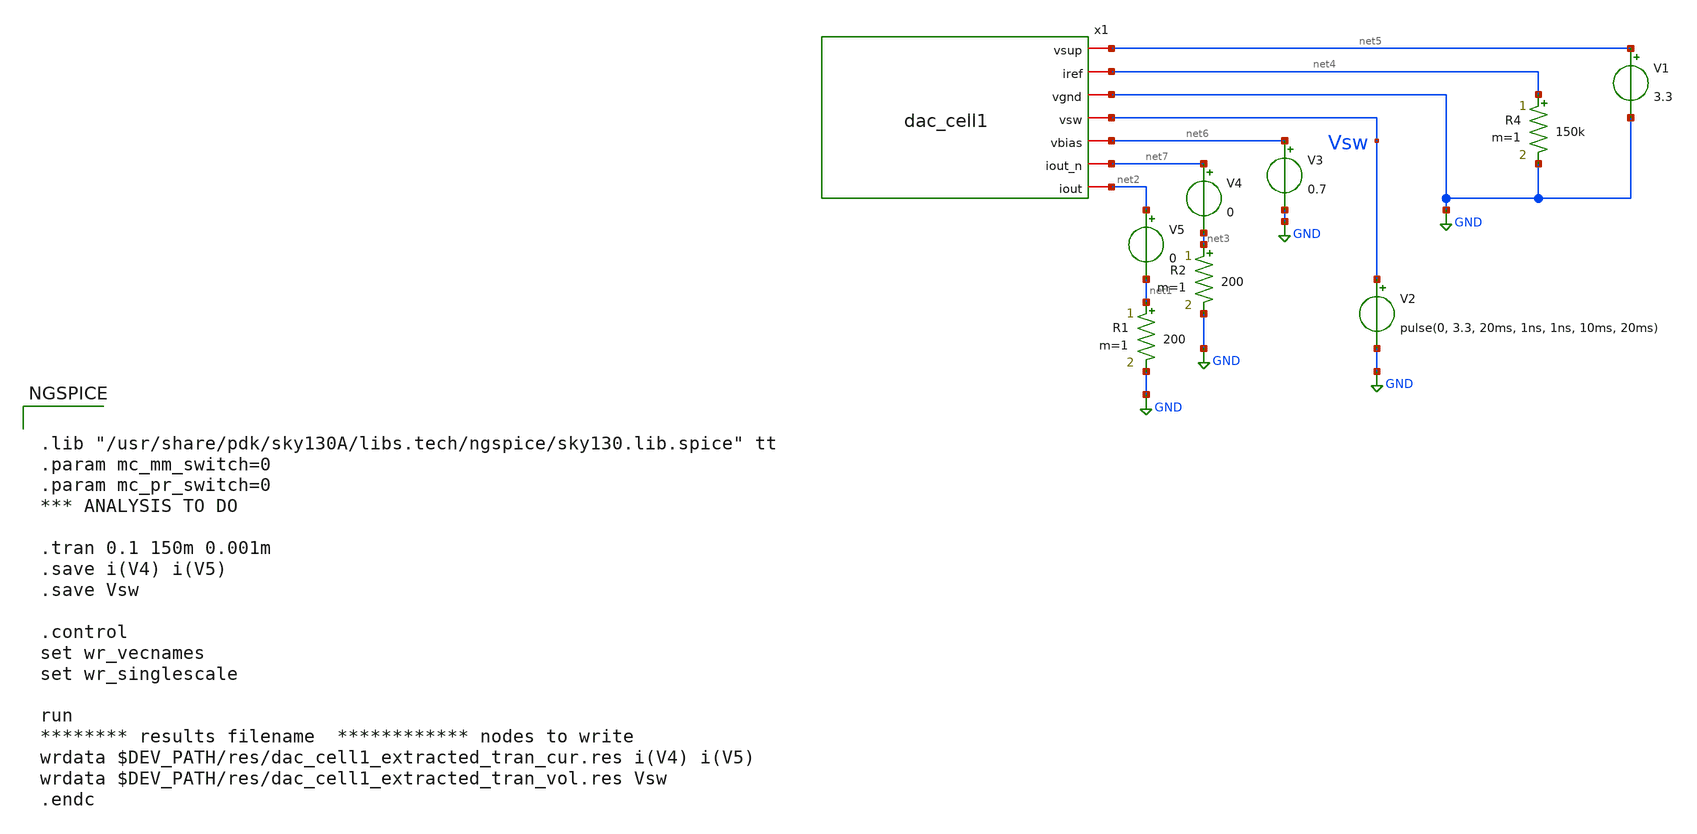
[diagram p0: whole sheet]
** sch_path: dev/dac_cell1/tb/tb_dac_cell1_tran_extracted.sch
**.subckt tb_dac_cell1_tran_extracted
V1 net5 GND 3.3
V2 Vsw GND pulse(0, 3.3, 20ms, 1ns, 1ns, 10ms, 20ms)
V3 net6 GND 0.7
V4 net7 net3 0
V5 net2 net1 0
R1 net1 GND 200 m=1
R2 net3 GND 200 m=1
R4 net4 GND 150k m=1
x1 net5 net4 GND Vsw net6 net7 net2 dac_cell1
**** begin user architecture code


.lib "/usr/share/pdk/sky130A/libs.tech/ngspice/sky130.lib.spice" tt
.param mc_mm_switch=0
.param mc_pr_switch=0
*** ANALYSIS TO DO

.tran 0.1 150m 0.001m
.save i(V4) i(V5)
.save Vsw

.control
set wr_vecnames
set wr_singlescale

run
******** results filename  ************ nodes to write
wrdata $DEV_PATH/res/dac_cell1_extracted_tran_cur.res i(V4) i(V5)
wrdata $DEV_PATH/res/dac_cell1_extracted_tran_vol.res Vsw
.endc


**** end user architecture code
**.ends
.GLOBAL GND
.end
